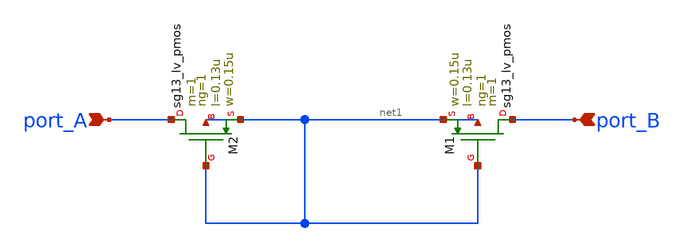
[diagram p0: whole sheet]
** sch_path: analog-db/templates/pseudo_resistor/pseudo-resistor-b-well-and-generator.sch
**.subckt pseudo-resistor-b-well-and-generator port_A port_B
*.ipin port_A
*.ipin port_B
XM1 port_B net1 net1 net1 sg13_lv_pmos w=0.15u l=0.13u ng=1 m=1 mm_ok=1
XM2 port_A net1 net1 net1 sg13_lv_pmos w=0.15u l=0.13u ng=1 m=1 mm_ok=1
**.ends
.end
